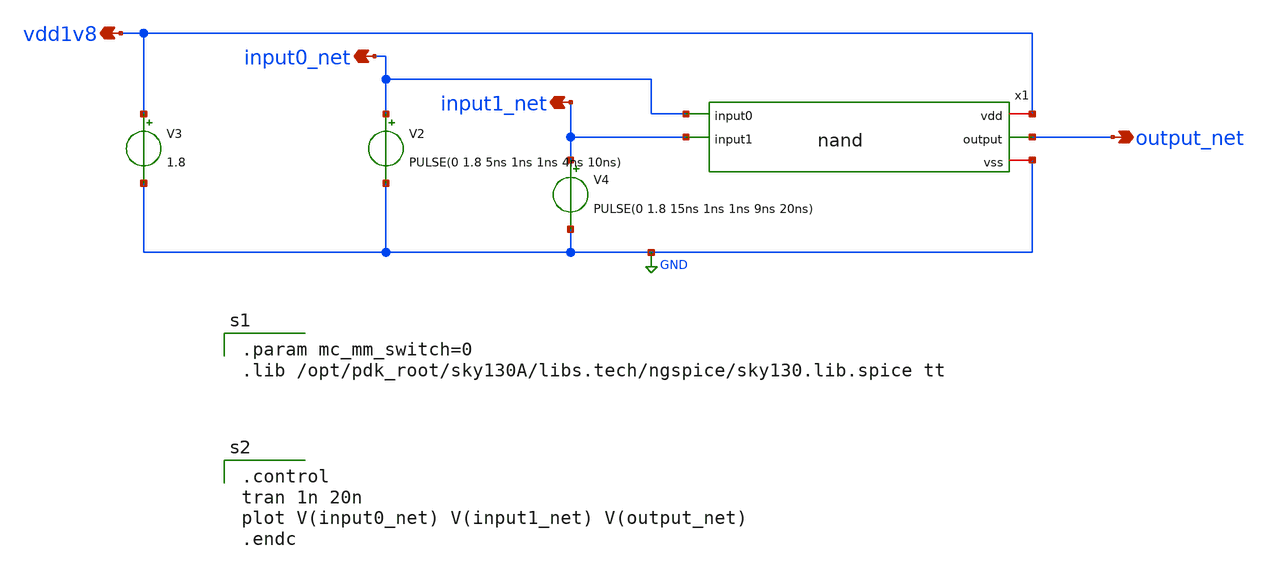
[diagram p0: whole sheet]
** sch_path: xschem/nand_tb.sch
**.subckt nand_tb input0_net vdd1v8 output_net input1_net
*.opin input0_net
*.opin vdd1v8
*.opin output_net
*.opin input1_net
V2 input0_net GND PULSE(0 1.8 5ns 1ns 1ns 4ns 10ns)
V3 vdd1v8 GND 1.8
V4 input1_net GND PULSE(0 1.8 15ns 1ns 1ns 9ns 20ns)
x1 vdd1v8 input0_net output_net input1_net GND nand
**** begin user architecture code

.param mc_mm_switch=0
.lib /opt/pdk_root/sky130A/libs.tech/ngspice/sky130.lib.spice tt


.control
tran 1n 20n
plot V(input0_net) V(input1_net) V(output_net)
.endc

**** end user architecture code
**.ends

* expanding   symbol:  nand.sym # of pins=5
** sym_path: xschem/nand.sym
** sch_path: xschem/nand.sch
.subckt nand vdd input0 output input1 vss
*.opin output
*.ipin input0
*.iopin vdd
*.ipin input1
*.iopin vss
XM1 output input1 net1 vss sky130_fd_pr__nfet_01v8 L=0.15 W=1 nf=1 ad='int((nf+1)/2) * W/nf * 0.29' as='int((nf+2)/2) * W/nf * 0.29'
+ pd='2*int((nf+1)/2) * (W/nf + 0.29)' ps='2*int((nf+2)/2) * (W/nf + 0.29)' nrd='0.29 / W' nrs='0.29 / W'
+ sa=0 sb=0 sd=0 mult=1 m=1
XM2 net1 input0 vss vss sky130_fd_pr__nfet_01v8 L=0.15 W=1 nf=1 ad='int((nf+1)/2) * W/nf * 0.29' as='int((nf+2)/2) * W/nf * 0.29'
+ pd='2*int((nf+1)/2) * (W/nf + 0.29)' ps='2*int((nf+2)/2) * (W/nf + 0.29)' nrd='0.29 / W' nrs='0.29 / W'
+ sa=0 sb=0 sd=0 mult=1 m=1
XM3 output input0 vdd vdd sky130_fd_pr__pfet_01v8 L=0.15 W=1 nf=1 ad='int((nf+1)/2) * W/nf * 0.29' as='int((nf+2)/2) * W/nf * 0.29'
+ pd='2*int((nf+1)/2) * (W/nf + 0.29)' ps='2*int((nf+2)/2) * (W/nf + 0.29)' nrd='0.29 / W' nrs='0.29 / W'
+ sa=0 sb=0 sd=0 mult=1 m=1
XM4 output input1 vdd vdd sky130_fd_pr__pfet_01v8 L=0.15 W=1 nf=1 ad='int((nf+1)/2) * W/nf * 0.29' as='int((nf+2)/2) * W/nf * 0.29'
+ pd='2*int((nf+1)/2) * (W/nf + 0.29)' ps='2*int((nf+2)/2) * (W/nf + 0.29)' nrd='0.29 / W' nrs='0.29 / W'
+ sa=0 sb=0 sd=0 mult=1 m=1
.ends

.GLOBAL GND
.end
